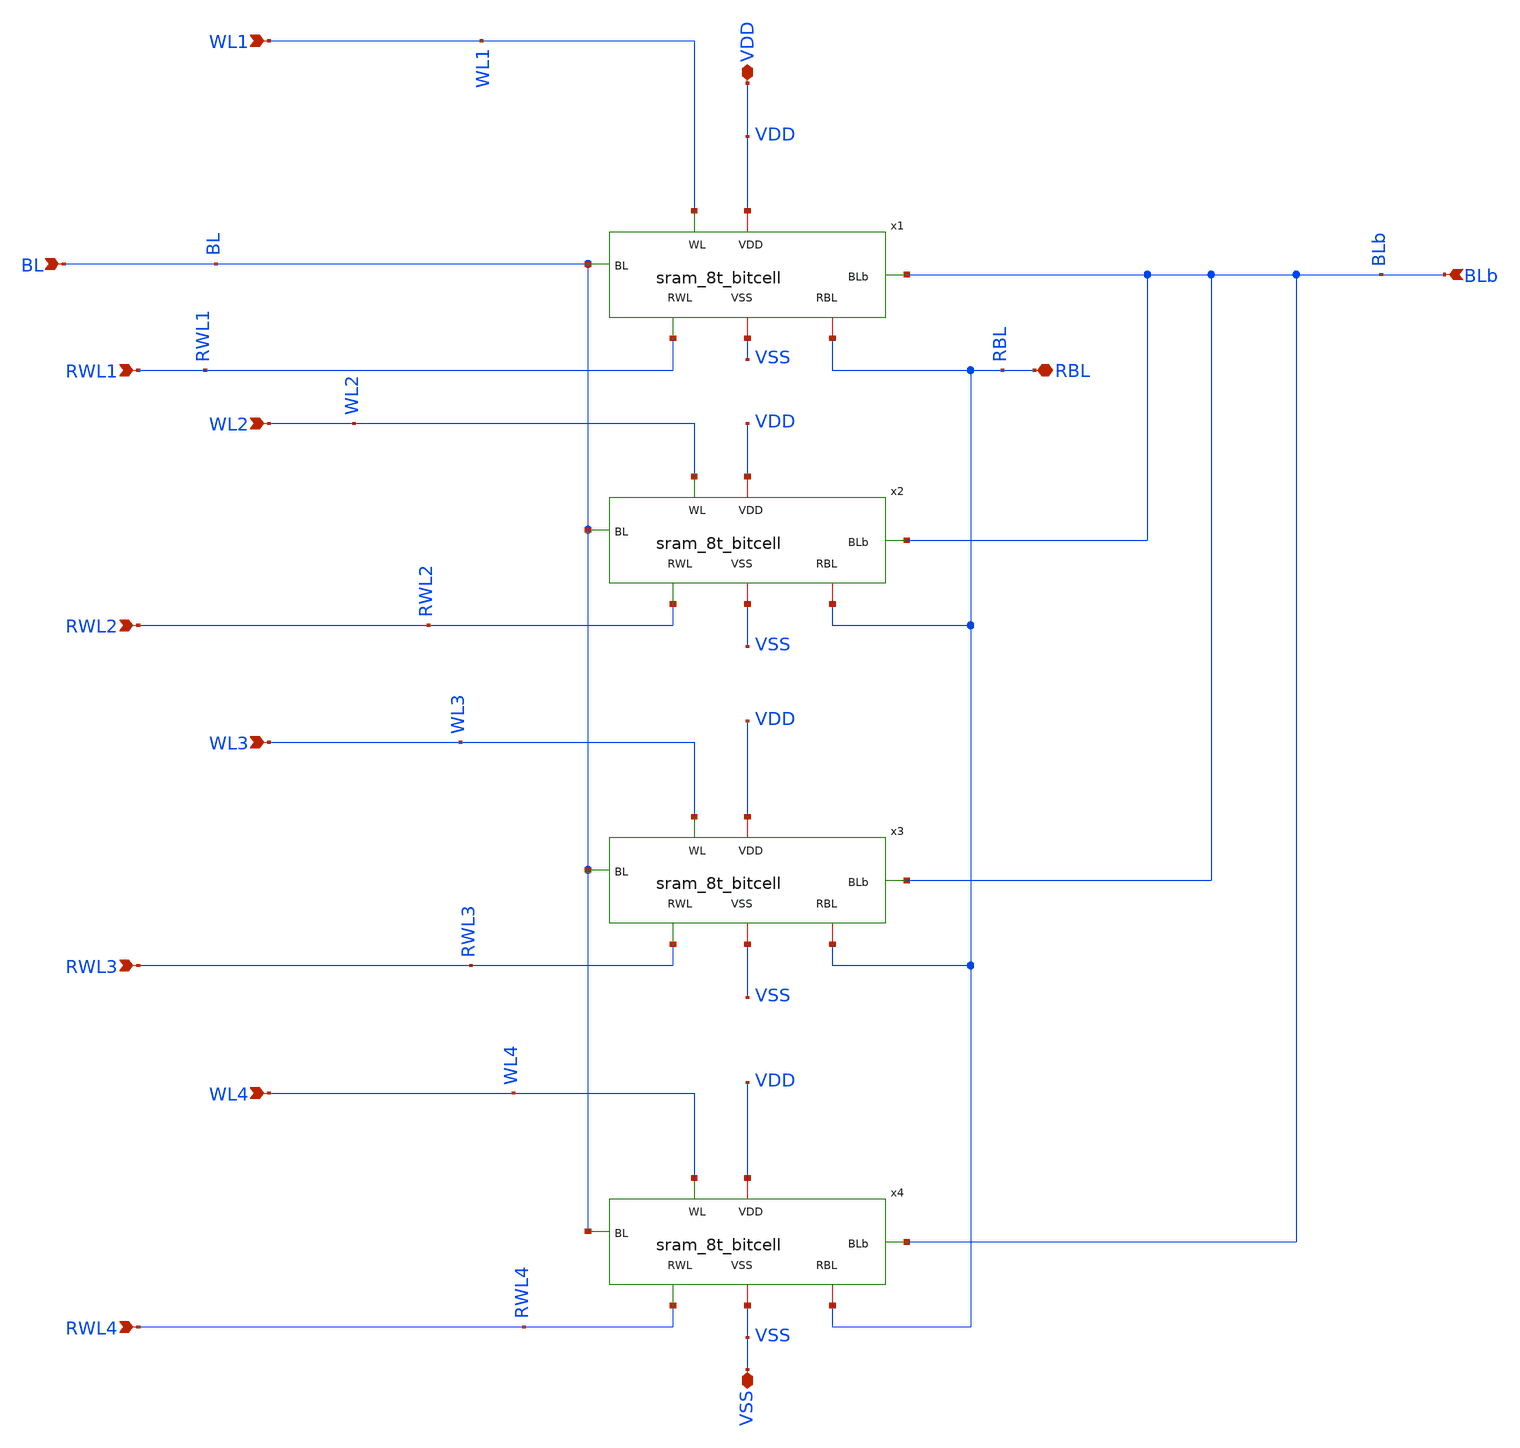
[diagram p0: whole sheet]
** sch_path: schematics/single_col_4cell.sch
**.subckt single_col_4cell RWL4 WL4 WL3 RWL3 WL2 RWL2 WL1 RWL1 BL BLb VDD RBL VSS
*.ipin RWL4
*.ipin WL4
*.ipin WL3
*.ipin RWL3
*.ipin WL2
*.ipin RWL2
*.ipin WL1
*.ipin RWL1
*.ipin BL
*.ipin BLb
*.iopin VDD
*.iopin RBL
*.iopin VSS
x1 VDD WL1 BL BLb RWL1 VSS RBL sram_8t_bitcell
x2 VDD WL2 BL BLb RWL2 VSS RBL sram_8t_bitcell
x3 VDD WL3 BL BLb RWL3 VSS RBL sram_8t_bitcell
x4 VDD WL4 BL BLb RWL4 VSS RBL sram_8t_bitcell
**.ends
.end
